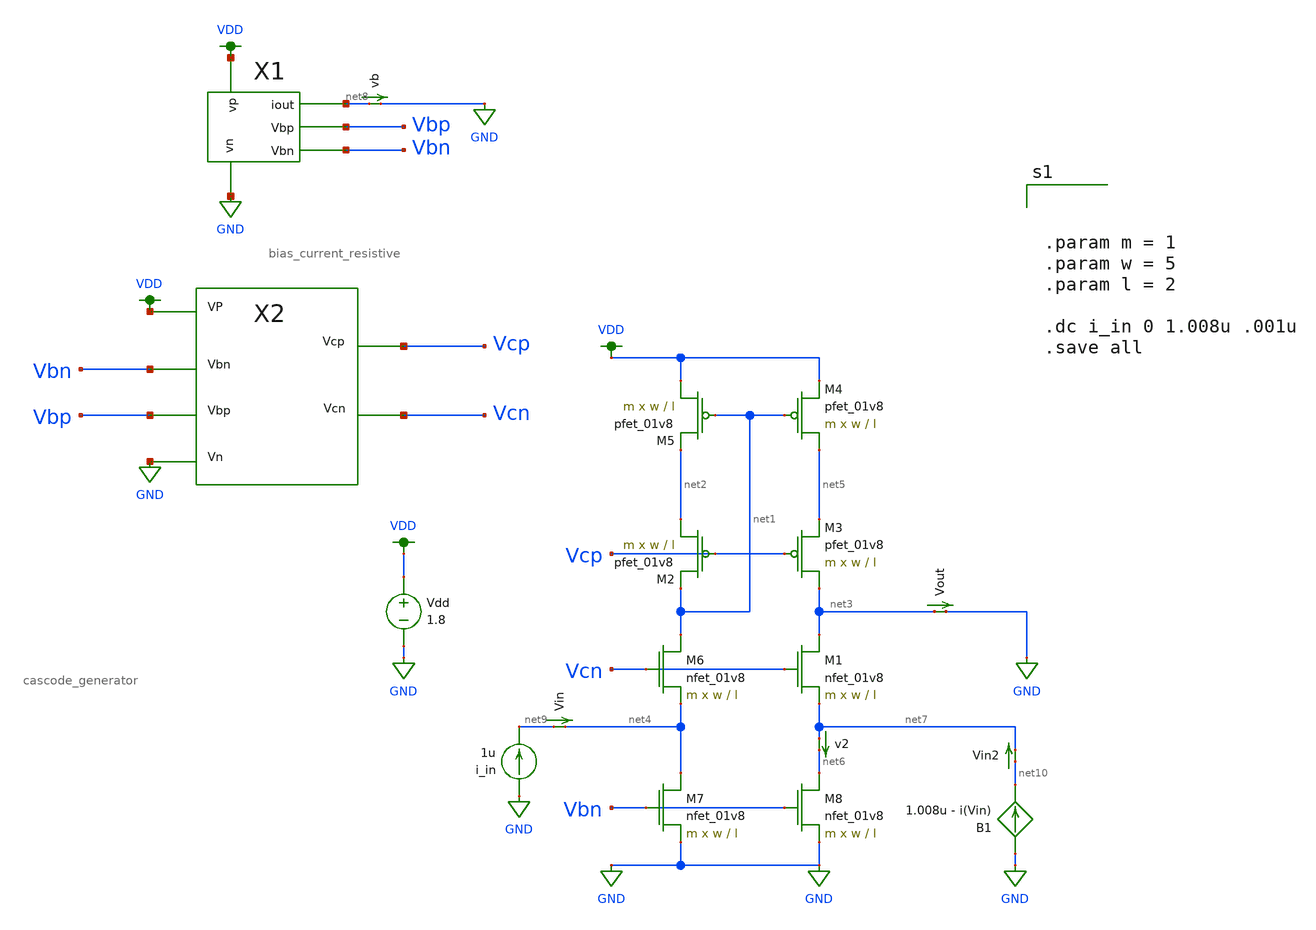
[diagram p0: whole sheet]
** sch_path: schematic/test/iout_mirror.sch
**.subckt iout_mirror
i_in GND net9 1u
XM5 VDD net1 net2 VDD sky130_fd_pr__pfet_01v8 L=l W=w nf=1 ad='int((nf+1)/2) * W/nf * 0.29' as='int((nf+2)/2) * W/nf * 0.29'
+ pd='2*int((nf+1)/2) * (W/nf + 0.29)' ps='2*int((nf+2)/2) * (W/nf + 0.29)' nrd='0.29 / W' nrs='0.29 / W'
+ sa=0 sb=0 sd=0 mult=m m=m
XM4 net5 net1 VDD VDD sky130_fd_pr__pfet_01v8 L=l W=w nf=1 ad='int((nf+1)/2) * W/nf * 0.29' as='int((nf+2)/2) * W/nf * 0.29'
+ pd='2*int((nf+1)/2) * (W/nf + 0.29)' ps='2*int((nf+2)/2) * (W/nf + 0.29)' nrd='0.29 / W' nrs='0.29 / W'
+ sa=0 sb=0 sd=0 mult=m m=m
XM2 net2 Vcp net1 VDD sky130_fd_pr__pfet_01v8 L=l W=w nf=1 ad='int((nf+1)/2) * W/nf * 0.29' as='int((nf+2)/2) * W/nf * 0.29'
+ pd='2*int((nf+1)/2) * (W/nf + 0.29)' ps='2*int((nf+2)/2) * (W/nf + 0.29)' nrd='0.29 / W' nrs='0.29 / W'
+ sa=0 sb=0 sd=0 mult=m m=m
XM3 net3 Vcp net5 VDD sky130_fd_pr__pfet_01v8 L=l W=w nf=1 ad='int((nf+1)/2) * W/nf * 0.29' as='int((nf+2)/2) * W/nf * 0.29'
+ pd='2*int((nf+1)/2) * (W/nf + 0.29)' ps='2*int((nf+2)/2) * (W/nf + 0.29)' nrd='0.29 / W' nrs='0.29 / W'
+ sa=0 sb=0 sd=0 mult=m m=m
XM1 net3 Vcn net7 GND sky130_fd_pr__nfet_01v8 L=l W=w nf=1 ad='int((nf+1)/2) * W/nf * 0.29' as='int((nf+2)/2) * W/nf * 0.29'
+ pd='2*int((nf+1)/2) * (W/nf + 0.29)' ps='2*int((nf+2)/2) * (W/nf + 0.29)' nrd='0.29 / W' nrs='0.29 / W'
+ sa=0 sb=0 sd=0 mult=m m=m
XM6 net1 Vcn net4 GND sky130_fd_pr__nfet_01v8 L=l W=w nf=1 ad='int((nf+1)/2) * W/nf * 0.29' as='int((nf+2)/2) * W/nf * 0.29'
+ pd='2*int((nf+1)/2) * (W/nf + 0.29)' ps='2*int((nf+2)/2) * (W/nf + 0.29)' nrd='0.29 / W' nrs='0.29 / W'
+ sa=0 sb=0 sd=0 mult=m m=m
XM7 net4 Vbn GND GND sky130_fd_pr__nfet_01v8 L=l W=w nf=1 ad='int((nf+1)/2) * W/nf * 0.29' as='int((nf+2)/2) * W/nf * 0.29'
+ pd='2*int((nf+1)/2) * (W/nf + 0.29)' ps='2*int((nf+2)/2) * (W/nf + 0.29)' nrd='0.29 / W' nrs='0.29 / W'
+ sa=0 sb=0 sd=0 mult=m m=m
XM8 net6 Vbn GND GND sky130_fd_pr__nfet_01v8 L=l W=w nf=1 ad='int((nf+1)/2) * W/nf * 0.29' as='int((nf+2)/2) * W/nf * 0.29'
+ pd='2*int((nf+1)/2) * (W/nf + 0.29)' ps='2*int((nf+2)/2) * (W/nf + 0.29)' nrd='0.29 / W' nrs='0.29 / W'
+ sa=0 sb=0 sd=0 mult=m m=m
Vdd VDD GND 1.8
Vout net3 GND 0
.save i(vout)
X1 VDD GND net8 Vbp Vbn bias_current_resistive
X2 VDD Vcn Vbn Vbp GND Vcp cascode_generator
v2 net7 net6 0
.save i(v2)
vb net8 GND 0
.save i(vb)
Vin net9 net4 0
.save i(vin)
B1 GND net10 I=1.008u - i(Vin)
Vin2 net10 net7 0
.save i(vin2)
**** begin user architecture code



.param m = 1
.param w = 5
.param l = 2

.dc i_in 0 1.008u .001u
.save all



.option wnflag=1
.param MC_SWITCH=0.0
.lib ~/skywater/skywater-pdk/libraries/sky130_fd_pr_ngspice/latest/models/sky130.lib.spice tt

**** end user architecture code
**.ends

* expanding   symbol:
*+  /home/madvlsi/Desktop/madvlsi/madvlsi_proj_4/schematic/bias_current_resistive.sym # of pins=5
** sym_path: schematic/bias_current_resistive.sym
** sch_path: schematic/bias_current_resistive.sch
.subckt bias_current_resistive vp vn iout Vbp Vbn
*.iopin vp
*.iopin vn
*.opin iout
*.opin Vbp
*.opin Vbn
XM1 vp Vbp net2 VDD sky130_fd_pr__pfet_01v8 L=l W=w nf=1 ad='int((nf+1)/2) * W/nf * 0.29' as='int((nf+2)/2) * W/nf * 0.29'
+ pd='2*int((nf+1)/2) * (W/nf + 0.29)' ps='2*int((nf+2)/2) * (W/nf + 0.29)' nrd='0.29 / W' nrs='0.29 / W'
+ sa=0 sb=0 sd=0 mult=1 m=1
XM2 vp net3 net3 VDD sky130_fd_pr__pfet_01v8 L=l W=w nf=1 ad='int((nf+1)/2) * W/nf * 0.29' as='int((nf+2)/2) * W/nf * 0.29'
+ pd='2*int((nf+1)/2) * (W/nf + 0.29)' ps='2*int((nf+2)/2) * (W/nf + 0.29)' nrd='0.29 / W' nrs='0.29 / W'
+ sa=0 sb=0 sd=0 mult=1 m=1
XM3 Vbp net3 vp VDD sky130_fd_pr__pfet_01v8 L=l W=w nf=1 ad='int((nf+1)/2) * W/nf * 0.29' as='int((nf+2)/2) * W/nf * 0.29'
+ pd='2*int((nf+1)/2) * (W/nf + 0.29)' ps='2*int((nf+2)/2) * (W/nf + 0.29)' nrd='0.29 / W' nrs='0.29 / W'
+ sa=0 sb=0 sd=0 mult=1 m=1
XM5 Vbn Vbp vp VDD sky130_fd_pr__pfet_01v8 L=l W=w nf=1 ad='int((nf+1)/2) * W/nf * 0.29' as='int((nf+2)/2) * W/nf * 0.29'
+ pd='2*int((nf+1)/2) * (W/nf + 0.29)' ps='2*int((nf+2)/2) * (W/nf + 0.29)' nrd='0.29 / W' nrs='0.29 / W'
+ sa=0 sb=0 sd=0 mult=1 m=1
XM4 net1 net2 net2 GND sky130_fd_pr__nfet_01v8 L=l W=w nf=1 ad='int((nf+1)/2) * W/nf * 0.29' as='int((nf+2)/2) * W/nf * 0.29'
+ pd='2*int((nf+1)/2) * (W/nf + 0.29)' ps='2*int((nf+2)/2) * (W/nf + 0.29)' nrd='0.29 / W' nrs='0.29 / W'
+ sa=0 sb=0 sd=0 mult=Mn m=Mn
XM6 net3 net2 vn GND sky130_fd_pr__nfet_01v8 L=l W=w nf=1 ad='int((nf+1)/2) * W/nf * 0.29' as='int((nf+2)/2) * W/nf * 0.29'
+ pd='2*int((nf+1)/2) * (W/nf + 0.29)' ps='2*int((nf+2)/2) * (W/nf + 0.29)' nrd='0.29 / W' nrs='0.29 / W'
+ sa=0 sb=0 sd=0 mult=1 m=1
XM7 vn Vbn Vbp GND sky130_fd_pr__nfet_01v8 L=l W=w nf=1 ad='int((nf+1)/2) * W/nf * 0.29' as='int((nf+2)/2) * W/nf * 0.29'
+ pd='2*int((nf+1)/2) * (W/nf + 0.29)' ps='2*int((nf+2)/2) * (W/nf + 0.29)' nrd='0.29 / W' nrs='0.29 / W'
+ sa=0 sb=0 sd=0 mult=1 m=1
XM8 Vbn Vbn vn GND sky130_fd_pr__nfet_01v8 L=l W=w nf=1 ad='int((nf+1)/2) * W/nf * 0.29' as='int((nf+2)/2) * W/nf * 0.29'
+ pd='2*int((nf+1)/2) * (W/nf + 0.29)' ps='2*int((nf+2)/2) * (W/nf + 0.29)' nrd='0.29 / W' nrs='0.29 / W'
+ sa=0 sb=0 sd=0 mult=1 m=1
R1 net1 vn 74k m=1
**** begin user architecture code


.param w=5
.param l=2
.param Mn=8


**** end user architecture code
XM9 iout Vbp vp VDD sky130_fd_pr__pfet_01v8 L=l W=w nf=1 ad='int((nf+1)/2) * W/nf * 0.29' as='int((nf+2)/2) * W/nf * 0.29'
+ pd='2*int((nf+1)/2) * (W/nf + 0.29)' ps='2*int((nf+2)/2) * (W/nf + 0.29)' nrd='0.29 / W' nrs='0.29 / W'
+ sa=0 sb=0 sd=0 mult=1 m=1
.ends


* expanding   symbol:  /home/madvlsi/Desktop/madvlsi/madvlsi_proj_4/schematic/cascode_generator.sym
*+ # of pins=6
** sym_path: schematic/cascode_generator.sym
** sch_path: schematic/cascode_generator.sch
.subckt cascode_generator Vp Vcn Vbn Vbp Vn Vcp
*.ipin Vbp
*.ipin Vbn
*.iopin Vn
*.iopin Vp
*.opin Vcp
*.opin Vcn
XM1 net2 Vbn Vn GND sky130_fd_pr__nfet_01v8 L=l W=w nf=1 ad='int((nf+1)/2) * W/nf * 0.29' as='int((nf+2)/2) * W/nf * 0.29'
+ pd='2*int((nf+1)/2) * (W/nf + 0.29)' ps='2*int((nf+2)/2) * (W/nf + 0.29)' nrd='0.29 / W' nrs='0.29 / W'
+ sa=0 sb=0 sd=0 mult=1 m=1
XM2 net1 net2 Vp VDD sky130_fd_pr__pfet_01v8 L=l W=w nf=1 ad='int((nf+1)/2) * W/nf * 0.29' as='int((nf+2)/2) * W/nf * 0.29'
+ pd='2*int((nf+1)/2) * (W/nf + 0.29)' ps='2*int((nf+2)/2) * (W/nf + 0.29)' nrd='0.29 / W' nrs='0.29 / W'
+ sa=0 sb=0 sd=0 mult=m m=m
XM3 Vn Vbn Vcp GND sky130_fd_pr__nfet_01v8 L=l W=w nf=1 ad='int((nf+1)/2) * W/nf * 0.29' as='int((nf+2)/2) * W/nf * 0.29'
+ pd='2*int((nf+1)/2) * (W/nf + 0.29)' ps='2*int((nf+2)/2) * (W/nf + 0.29)' nrd='0.29 / W' nrs='0.29 / W'
+ sa=0 sb=0 sd=0 mult=1 m=1
XM4 net2 net2 net1 VDD sky130_fd_pr__pfet_01v8 L=l W=w nf=1 ad='int((nf+1)/2) * W/nf * 0.29' as='int((nf+2)/2) * W/nf * 0.29'
+ pd='2*int((nf+1)/2) * (W/nf + 0.29)' ps='2*int((nf+2)/2) * (W/nf + 0.29)' nrd='0.29 / W' nrs='0.29 / W'
+ sa=0 sb=0 sd=0 mult=m*4 m=m*4
XM5 net1 Vcp Vcp VDD sky130_fd_pr__pfet_01v8 L=l W=w nf=1 ad='int((nf+1)/2) * W/nf * 0.29' as='int((nf+2)/2) * W/nf * 0.29'
+ pd='2*int((nf+1)/2) * (W/nf + 0.29)' ps='2*int((nf+2)/2) * (W/nf + 0.29)' nrd='0.29 / W' nrs='0.29 / W'
+ sa=0 sb=0 sd=0 mult=1 m=1
XM6 net3 net3 net4 GND sky130_fd_pr__nfet_01v8 L=l W=w nf=1 ad='int((nf+1)/2) * W/nf * 0.29' as='int((nf+2)/2) * W/nf * 0.29'
+ pd='2*int((nf+1)/2) * (W/nf + 0.29)' ps='2*int((nf+2)/2) * (W/nf + 0.29)' nrd='0.29 / W' nrs='0.29 / W'
+ sa=0 sb=0 sd=0 mult=m*4 m=m*4
XM7 net4 Vcn Vcn GND sky130_fd_pr__nfet_01v8 L=l W=w nf=1 ad='int((nf+1)/2) * W/nf * 0.29' as='int((nf+2)/2) * W/nf * 0.29'
+ pd='2*int((nf+1)/2) * (W/nf + 0.29)' ps='2*int((nf+2)/2) * (W/nf + 0.29)' nrd='0.29 / W' nrs='0.29 / W'
+ sa=0 sb=0 sd=0 mult=m m=m
XM8 net3 Vbp Vp VDD sky130_fd_pr__pfet_01v8 L=l W=w nf=1 ad='int((nf+1)/2) * W/nf * 0.29' as='int((nf+2)/2) * W/nf * 0.29'
+ pd='2*int((nf+1)/2) * (W/nf + 0.29)' ps='2*int((nf+2)/2) * (W/nf + 0.29)' nrd='0.29 / W' nrs='0.29 / W'
+ sa=0 sb=0 sd=0 mult=1 m=1
XM9 Vp Vbp Vcn VDD sky130_fd_pr__pfet_01v8 L=l W=w nf=1 ad='int((nf+1)/2) * W/nf * 0.29' as='int((nf+2)/2) * W/nf * 0.29'
+ pd='2*int((nf+1)/2) * (W/nf + 0.29)' ps='2*int((nf+2)/2) * (W/nf + 0.29)' nrd='0.29 / W' nrs='0.29 / W'
+ sa=0 sb=0 sd=0 mult=m m=m
XM10 net4 net3 Vn GND sky130_fd_pr__nfet_01v8 L=l W=w nf=1 ad='int((nf+1)/2) * W/nf * 0.29' as='int((nf+2)/2) * W/nf * 0.29'
+ pd='2*int((nf+1)/2) * (W/nf + 0.29)' ps='2*int((nf+2)/2) * (W/nf + 0.29)' nrd='0.29 / W' nrs='0.29 / W'
+ sa=0 sb=0 sd=0 mult=m m=m
**** begin user architecture code


.param w=5
.param l=2
.param m=5


**** end user architecture code
.ends

.GLOBAL GND
.GLOBAL VDD
.end
